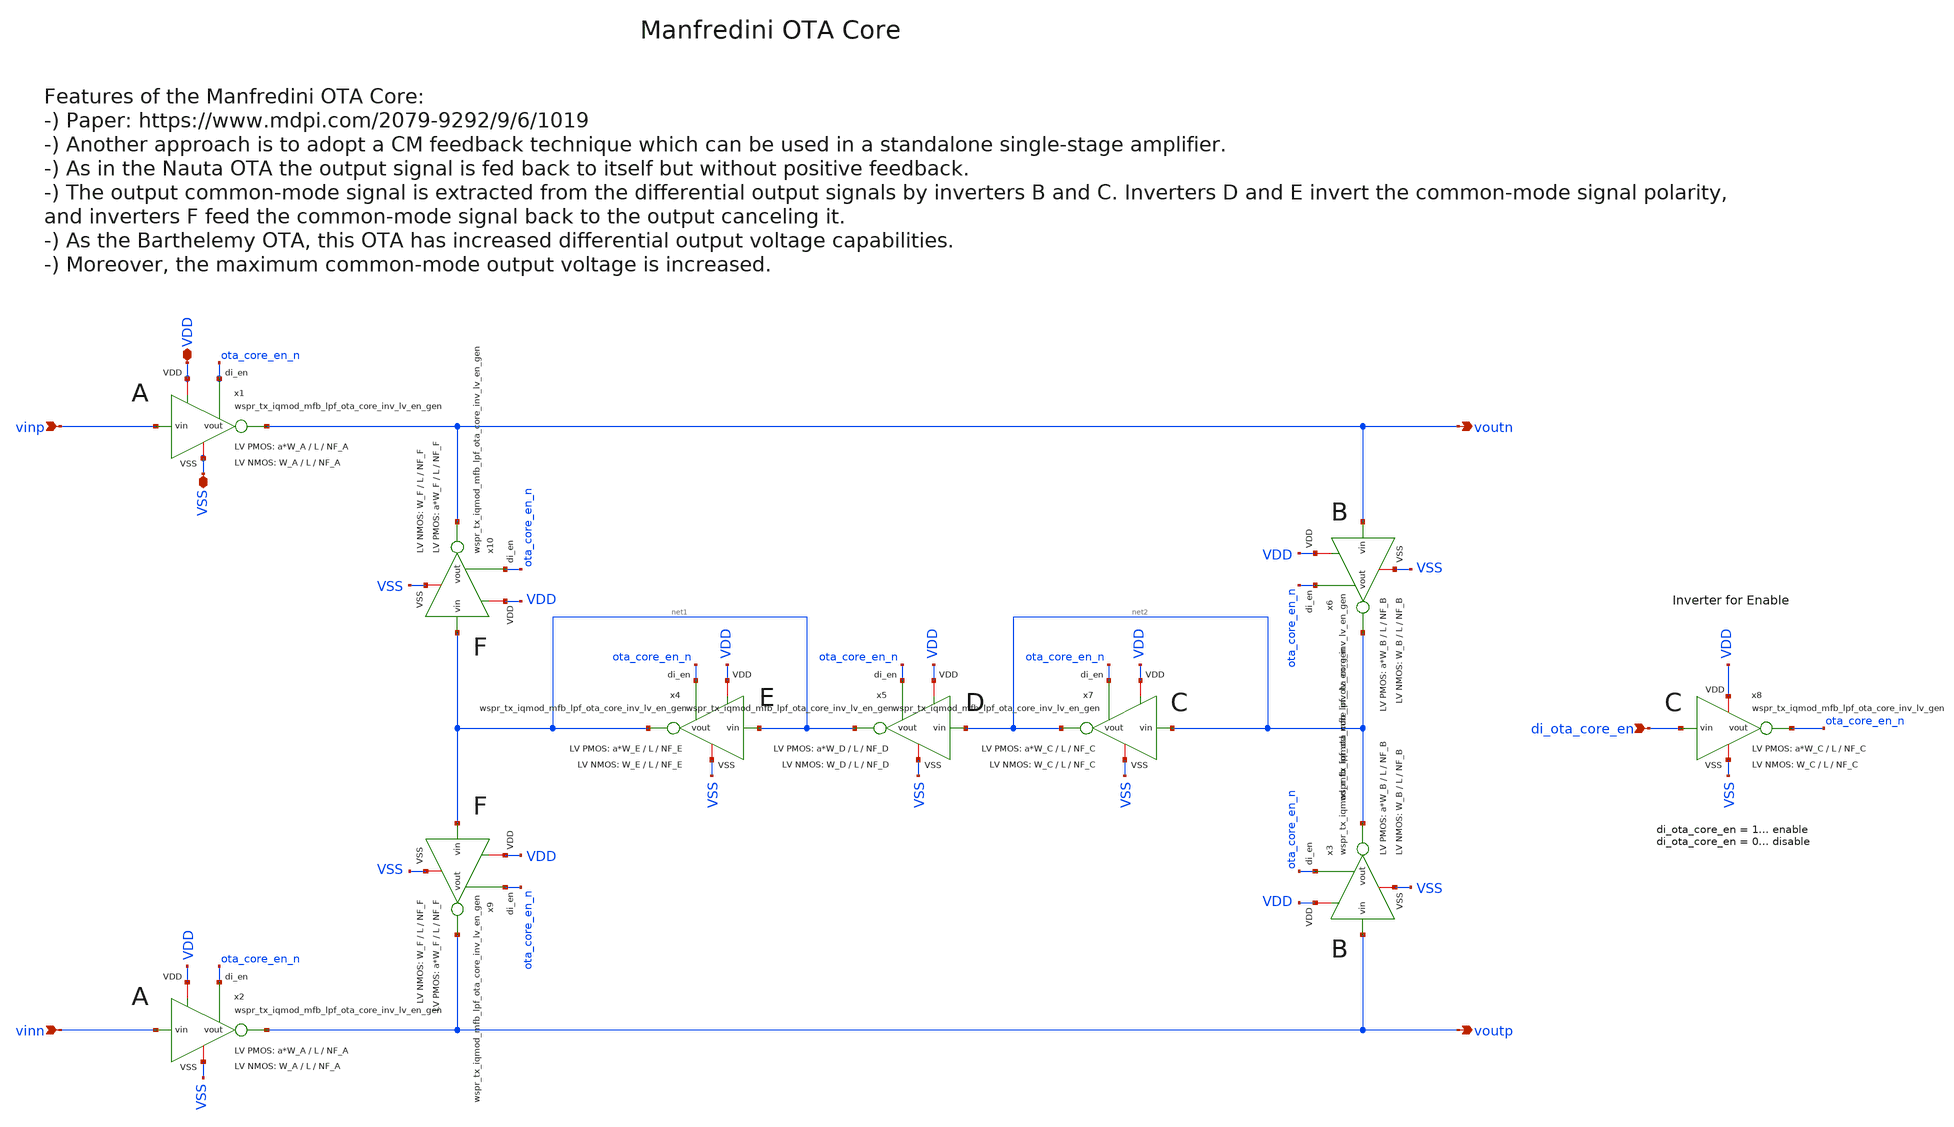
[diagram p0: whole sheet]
** sch_path: sky130/xschem/generic/wspr_tx_iqmod_mfb_lpf_ota_core_manfredini_gen.sch
**.subckt wspr_tx_iqmod_mfb_lpf_ota_core_manfredini_gen di_ota_core_en vinp vinn voutp voutn VDD VSS
*.ipin di_ota_core_en
*.ipin vinp
*.ipin vinn
*.opin voutp
*.opin voutn
*.iopin VDD
*.iopin VSS
x2 VDD vinn voutp VSS ota_core_en_n wspr_tx_iqmod_mfb_lpf_ota_core_inv_lv_en_gen W_P=a*W_A L_P=L
+ NF_P=NF_A W_N=W_A L_N=L NF_N=NF_A
x1 VDD vinp voutn VSS ota_core_en_n wspr_tx_iqmod_mfb_lpf_ota_core_inv_lv_en_gen W_P=a*W_A L_P=L
+ NF_P=NF_A W_N=W_A L_N=L NF_N=NF_A
x4 VDD net1 net1 VSS ota_core_en_n wspr_tx_iqmod_mfb_lpf_ota_core_inv_lv_en_gen W_P=a*W_E L_P=L
+ NF_P=NF_E W_N=W_E L_N=L NF_N=NF_E
x5 VDD net2 net1 VSS ota_core_en_n wspr_tx_iqmod_mfb_lpf_ota_core_inv_lv_en_gen W_P=a*W_D L_P=L
+ NF_P=NF_D W_N=W_D L_N=L NF_N=NF_D
x6 VDD voutn net2 VSS ota_core_en_n wspr_tx_iqmod_mfb_lpf_ota_core_inv_lv_en_gen W_P=a*W_B L_P=L
+ NF_P=NF_B W_N=W_B L_N=L NF_N=NF_B
x3 VDD voutp net2 VSS ota_core_en_n wspr_tx_iqmod_mfb_lpf_ota_core_inv_lv_en_gen W_P=a*W_B L_P=L
+ NF_P=NF_B W_N=W_B L_N=L NF_N=NF_B
x7 VDD net2 net2 VSS ota_core_en_n wspr_tx_iqmod_mfb_lpf_ota_core_inv_lv_en_gen W_P=a*W_C L_P=L
+ NF_P=NF_C W_N=W_C L_N=L NF_N=NF_C
x8 VDD di_ota_core_en ota_core_en_n VSS wspr_tx_iqmod_mfb_lpf_ota_core_inv_lv_gen W_P=a*W_C L_P=L
+ NF_P=NF_C W_N=W_C L_N=L NF_N=NF_C
x9 VDD net1 voutp VSS ota_core_en_n wspr_tx_iqmod_mfb_lpf_ota_core_inv_lv_en_gen W_P=a*W_F L_P=L
+ NF_P=NF_F W_N=W_F L_N=L NF_N=NF_F
x10 VDD net1 voutn VSS ota_core_en_n wspr_tx_iqmod_mfb_lpf_ota_core_inv_lv_en_gen W_P=a*W_F L_P=L
+ NF_P=NF_F W_N=W_F L_N=L NF_N=NF_F
**.ends
.end
